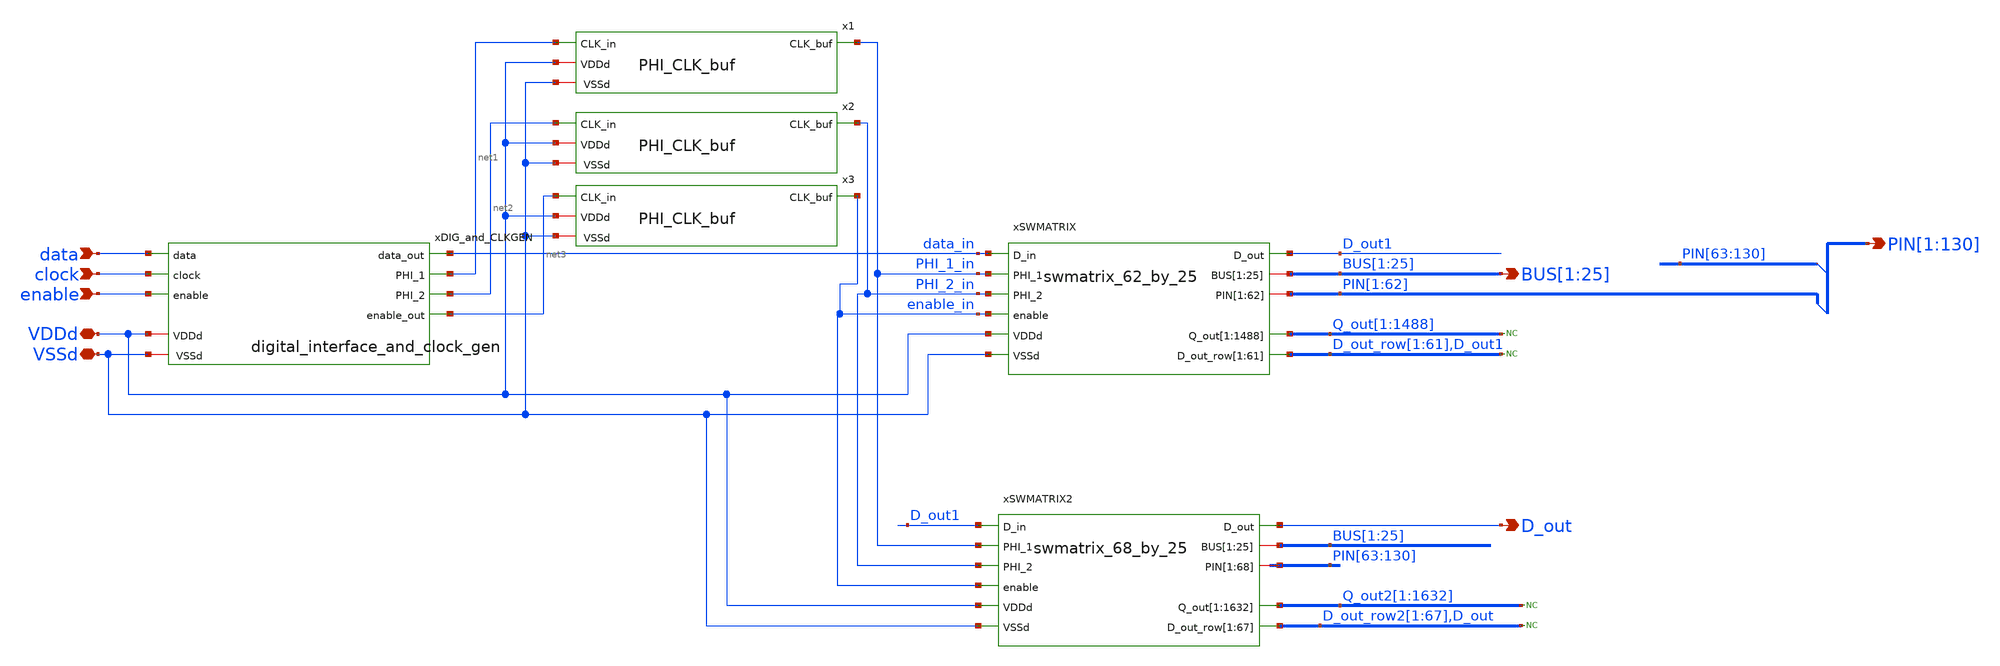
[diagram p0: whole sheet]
** sch_path: full_switch_matrix_130_by_25/full_switch_matrix_130_by_25_no_probes.sch
**.subckt full_switch_matrix_130_by_25_no_probes data clock enable D_out
*+ PIN[1],PIN[2],PIN[3],PIN[4],PIN[5],PIN[6],PIN[7],PIN[8],PIN[9],PIN[10],PIN[11],PIN[12],PIN[13],PIN[14],PIN[15],PIN[16],PIN[17],PIN[18],PIN[19],PIN[20],PIN[21],PIN[22],PIN[23],PIN[24],PIN[25],PIN[26],PIN[27],PIN[28],PIN[29],PIN[30],PIN[31],PIN[32],PIN[33],PIN[34],PIN[35],PIN[36],PIN[37],PIN[38],PIN[39],PIN[40],PIN[41],PIN[42],PIN[43],PIN[44],PIN[45],PIN[46],PIN[47],PIN[48],PIN[49],PIN[50],PIN[51],PIN[52],PIN[53],PIN[54],PIN[55],PIN[56],PIN[57],PIN[58],PIN[59],PIN[60],PIN[61],PIN[62],PIN[63],PIN[64],PIN[65],PIN[66],PIN[67],PIN[68],PIN[69],PIN[70],PIN[71],PIN[72],PIN[73],PIN[74],PIN[75],PIN[76],PIN[77],PIN[78],PIN[79],PIN[80],PIN[81],PIN[82],PIN[83],PIN[84],PIN[85],PIN[86],PIN[87],PIN[88],PIN[89],PIN[90],PIN[91],PIN[92],PIN[93],PIN[94],PIN[95],PIN[96],PIN[97],PIN[98],PIN[99],PIN[100],PIN[101],PIN[102],PIN[103],PIN[104],PIN[105],PIN[106],PIN[107],PIN[108],PIN[109],PIN[110],PIN[111],PIN[112],PIN[113],PIN[114],PIN[115],PIN[116],PIN[117],PIN[118],PIN[119],PIN[120],PIN[121],PIN[122],PIN[123],PIN[124],PIN[125],PIN[126],PIN[127],PIN[128],PIN[129],PIN[130]
*+ BUS[1],BUS[2],BUS[3],BUS[4],BUS[5],BUS[6],BUS[7],BUS[8],BUS[9],BUS[10],BUS[11],BUS[12],BUS[13],BUS[14],BUS[15],BUS[16],BUS[17],BUS[18],BUS[19],BUS[20],BUS[21],BUS[22],BUS[23],BUS[24],BUS[25] VSSd VDDd
*.ipin data
*.ipin clock
*.ipin enable
*.opin D_out
*.opin
*+ PIN[1],PIN[2],PIN[3],PIN[4],PIN[5],PIN[6],PIN[7],PIN[8],PIN[9],PIN[10],PIN[11],PIN[12],PIN[13],PIN[14],PIN[15],PIN[16],PIN[17],PIN[18],PIN[19],PIN[20],PIN[21],PIN[22],PIN[23],PIN[24],PIN[25],PIN[26],PIN[27],PIN[28],PIN[29],PIN[30],PIN[31],PIN[32],PIN[33],PIN[34],PIN[35],PIN[36],PIN[37],PIN[38],PIN[39],PIN[40],PIN[41],PIN[42],PIN[43],PIN[44],PIN[45],PIN[46],PIN[47],PIN[48],PIN[49],PIN[50],PIN[51],PIN[52],PIN[53],PIN[54],PIN[55],PIN[56],PIN[57],PIN[58],PIN[59],PIN[60],PIN[61],PIN[62],PIN[63],PIN[64],PIN[65],PIN[66],PIN[67],PIN[68],PIN[69],PIN[70],PIN[71],PIN[72],PIN[73],PIN[74],PIN[75],PIN[76],PIN[77],PIN[78],PIN[79],PIN[80],PIN[81],PIN[82],PIN[83],PIN[84],PIN[85],PIN[86],PIN[87],PIN[88],PIN[89],PIN[90],PIN[91],PIN[92],PIN[93],PIN[94],PIN[95],PIN[96],PIN[97],PIN[98],PIN[99],PIN[100],PIN[101],PIN[102],PIN[103],PIN[104],PIN[105],PIN[106],PIN[107],PIN[108],PIN[109],PIN[110],PIN[111],PIN[112],PIN[113],PIN[114],PIN[115],PIN[116],PIN[117],PIN[118],PIN[119],PIN[120],PIN[121],PIN[122],PIN[123],PIN[124],PIN[125],PIN[126],PIN[127],PIN[128],PIN[129],PIN[130]
*.opin
*+ BUS[1],BUS[2],BUS[3],BUS[4],BUS[5],BUS[6],BUS[7],BUS[8],BUS[9],BUS[10],BUS[11],BUS[12],BUS[13],BUS[14],BUS[15],BUS[16],BUS[17],BUS[18],BUS[19],BUS[20],BUS[21],BUS[22],BUS[23],BUS[24],BUS[25]
*.iopin VSSd
*.iopin VDDd
xSWMATRIX data_in D_out1 PHI_1_in PHI_2_in BUS[1] BUS[2] BUS[3] BUS[4] BUS[5] BUS[6] BUS[7] BUS[8]
+ BUS[9] BUS[10] BUS[11] BUS[12] BUS[13] BUS[14] BUS[15] BUS[16] BUS[17] BUS[18] BUS[19] BUS[20] BUS[21]
+ BUS[22] BUS[23] BUS[24] BUS[25] PIN[1] PIN[2] PIN[3] PIN[4] PIN[5] PIN[6] PIN[7] PIN[8] PIN[9] PIN[10]
+ PIN[11] PIN[12] PIN[13] PIN[14] PIN[15] PIN[16] PIN[17] PIN[18] PIN[19] PIN[20] PIN[21] PIN[22] PIN[23]
+ PIN[24] PIN[25] PIN[26] PIN[27] PIN[28] PIN[29] PIN[30] PIN[31] PIN[32] PIN[33] PIN[34] PIN[35] PIN[36]
+ PIN[37] PIN[38] PIN[39] PIN[40] PIN[41] PIN[42] PIN[43] PIN[44] PIN[45] PIN[46] PIN[47] PIN[48] PIN[49]
+ PIN[50] PIN[51] PIN[52] PIN[53] PIN[54] PIN[55] PIN[56] PIN[57] PIN[58] PIN[59] PIN[60] PIN[61] PIN[62]
+ VDDd VSSd enable_in Q_out[1] Q_out[2] Q_out[3] Q_out[4] Q_out[5] Q_out[6] Q_out[7] Q_out[8] Q_out[9]
+ Q_out[10] Q_out[11] Q_out[12] Q_out[13] Q_out[14] Q_out[15] Q_out[16] Q_out[17] Q_out[18] Q_out[19] Q_out[20]
+ Q_out[21] Q_out[22] Q_out[23] Q_out[24] Q_out[25] Q_out[26] Q_out[27] Q_out[28] Q_out[29] Q_out[30] Q_out[31]
+ Q_out[32] Q_out[33] Q_out[34] Q_out[35] Q_out[36] Q_out[37] Q_out[38] Q_out[39] Q_out[40] Q_out[41] Q_out[42]
+ Q_out[43] Q_out[44] Q_out[45] Q_out[46] Q_out[47] Q_out[48] Q_out[49] Q_out[50] Q_out[51] Q_out[52] Q_out[53]
+ Q_out[54] Q_out[55] Q_out[56] Q_out[57] Q_out[58] Q_out[59] Q_out[60] Q_out[61] Q_out[62] Q_out[63] Q_out[64]
+ Q_out[65] Q_out[66] Q_out[67] Q_out[68] Q_out[69] Q_out[70] Q_out[71] Q_out[72] Q_out[73] Q_out[74] Q_out[75]
+ Q_out[76] Q_out[77] Q_out[78] Q_out[79] Q_out[80] Q_out[81] Q_out[82] Q_out[83] Q_out[84] Q_out[85] Q_out[86]
+ Q_out[87] Q_out[88] Q_out[89] Q_out[90] Q_out[91] Q_out[92] Q_out[93] Q_out[94] Q_out[95] Q_out[96] Q_out[97]
+ Q_out[98] Q_out[99] Q_out[100] Q_out[101] Q_out[102] Q_out[103] Q_out[104] Q_out[105] Q_out[106] Q_out[107]
+ Q_out[108] Q_out[109] Q_out[110] Q_out[111] Q_out[112] Q_out[113] Q_out[114] Q_out[115] Q_out[116] Q_out[117]
+ Q_out[118] Q_out[119] Q_out[120] Q_out[121] Q_out[122] Q_out[123] Q_out[124] Q_out[125] Q_out[126] Q_out[127]
+ Q_out[128] Q_out[129] Q_out[130] Q_out[131] Q_out[132] Q_out[133] Q_out[134] Q_out[135] Q_out[136] Q_out[137]
+ Q_out[138] Q_out[139] Q_out[140] Q_out[141] Q_out[142] Q_out[143] Q_out[144] Q_out[145] Q_out[146] Q_out[147]
+ Q_out[148] Q_out[149] Q_out[150] Q_out[151] Q_out[152] Q_out[153] Q_out[154] Q_out[155] Q_out[156] Q_out[157]
+ Q_out[158] Q_out[159] Q_out[160] Q_out[161] Q_out[162] Q_out[163] Q_out[164] Q_out[165] Q_out[166] Q_out[167]
+ Q_out[168] Q_out[169] Q_out[170] Q_out[171] Q_out[172] Q_out[173] Q_out[174] Q_out[175] Q_out[176] Q_out[177]
+ Q_out[178] Q_out[179] Q_out[180] Q_out[181] Q_out[182] Q_out[183] Q_out[184] Q_out[185] Q_out[186] Q_out[187]
+ Q_out[188] Q_out[189] Q_out[190] Q_out[191] Q_out[192] Q_out[193] Q_out[194] Q_out[195] Q_out[196] Q_out[197]
+ Q_out[198] Q_out[199] Q_out[200] Q_out[201] Q_out[202] Q_out[203] Q_out[204] Q_out[205] Q_out[206] Q_out[207]
+ Q_out[208] Q_out[209] Q_out[210] Q_out[211] Q_out[212] Q_out[213] Q_out[214] Q_out[215] Q_out[216] Q_out[217]
+ Q_out[218] Q_out[219] Q_out[220] Q_out[221] Q_out[222] Q_out[223] Q_out[224] Q_out[225] Q_out[226] Q_out[227]
+ Q_out[228] Q_out[229] Q_out[230] Q_out[231] Q_out[232] Q_out[233] Q_out[234] Q_out[235] Q_out[236] Q_out[237]
+ Q_out[238] Q_out[239] Q_out[240] Q_out[241] Q_out[242] Q_out[243] Q_out[244] Q_out[245] Q_out[246] Q_out[247]
+ Q_out[248] Q_out[249] Q_out[250] Q_out[251] Q_out[252] Q_out[253] Q_out[254] Q_out[255] Q_out[256] Q_out[257]
+ Q_out[258] Q_out[259] Q_out[260] Q_out[261] Q_out[262] Q_out[263] Q_out[264] Q_out[265] Q_out[266] Q_out[267]
+ Q_out[268] Q_out[269] Q_out[270] Q_out[271] Q_out[272] Q_out[273] Q_out[274] Q_out[275] Q_out[276] Q_out[277]
+ Q_out[278] Q_out[279] Q_out[280] Q_out[281] Q_out[282] Q_out[283] Q_out[284] Q_out[285] Q_out[286] Q_out[287]
+ Q_out[288] Q_out[289] Q_out[290] Q_out[291] Q_out[292] Q_out[293] Q_out[294] Q_out[295] Q_out[296] Q_out[297]
+ Q_out[298] Q_out[299] Q_out[300] Q_out[301] Q_out[302] Q_out[303] Q_out[304] Q_out[305] Q_out[306] Q_out[307]
+ Q_out[308] Q_out[309] Q_out[310] Q_out[311] Q_out[312] Q_out[313] Q_out[314] Q_out[315] Q_out[316] Q_out[317]
+ Q_out[318] Q_out[319] Q_out[320] Q_out[321] Q_out[322] Q_out[323] Q_out[324] Q_out[325] Q_out[326] Q_out[327]
+ Q_out[328] Q_out[329] Q_out[330] Q_out[331] Q_out[332] Q_out[333] Q_out[334] Q_out[335] Q_out[336] Q_out[337]
+ Q_out[338] Q_out[339] Q_out[340] Q_out[341] Q_out[342] Q_out[343] Q_out[344] Q_out[345] Q_out[346] Q_out[347]
+ Q_out[348] Q_out[349] Q_out[350] Q_out[351] Q_out[352] Q_out[353] Q_out[354] Q_out[355] Q_out[356] Q_out[357]
+ Q_out[358] Q_out[359] Q_out[360] Q_out[361] Q_out[362] Q_out[363] Q_out[364] Q_out[365] Q_out[366] Q_out[367]
+ Q_out[368] Q_out[369] Q_out[370] Q_out[371] Q_out[372] Q_out[373] Q_out[374] Q_out[375] Q_out[376] Q_out[377]
+ Q_out[378] Q_out[379] Q_out[380] Q_out[381] Q_out[382] Q_out[383] Q_out[384] Q_out[385] Q_out[386] Q_out[387]
+ Q_out[388] Q_out[389] Q_out[390] Q_out[391] Q_out[392] Q_out[393] Q_out[394] Q_out[395] Q_out[396] Q_out[397]
+ Q_out[398] Q_out[399] Q_out[400] Q_out[401] Q_out[402] Q_out[403] Q_out[404] Q_out[405] Q_out[406] Q_out[407]
+ Q_out[408] Q_out[409] Q_out[410] Q_out[411] Q_out[412] Q_out[413] Q_out[414] Q_out[415] Q_out[416] Q_out[417]
+ Q_out[418] Q_out[419] Q_out[420] Q_out[421] Q_out[422] Q_out[423] Q_out[424] Q_out[425] Q_out[426] Q_out[427]
+ Q_out[428] Q_out[429] Q_out[430] Q_out[431] Q_out[432] Q_out[433] Q_out[434] Q_out[435] Q_out[436] Q_out[437]
+ Q_out[438] Q_out[439] Q_out[440] Q_out[441] Q_out[442] Q_out[443] Q_out[444] Q_out[445] Q_out[446] Q_out[447]
+ Q_out[448] Q_out[449] Q_out[450] Q_out[451] Q_out[452] Q_out[453] Q_out[454] Q_out[455] Q_out[456] Q_out[457]
+ Q_out[458] Q_out[459] Q_out[460] Q_out[461] Q_out[462] Q_out[463] Q_out[464] Q_out[465] Q_out[466] Q_out[467]
+ Q_out[468] Q_out[469] Q_out[470] Q_out[471] Q_out[472] Q_out[473] Q_out[474] Q_out[475] Q_out[476] Q_out[477]
+ Q_out[478] Q_out[479] Q_out[480] Q_out[481] Q_out[482] Q_out[483] Q_out[484] Q_out[485] Q_out[486] Q_out[487]
+ Q_out[488] Q_out[489] Q_out[490] Q_out[491] Q_out[492] Q_out[493] Q_out[494] Q_out[495] Q_out[496] Q_out[497]
+ Q_out[498] Q_out[499] Q_out[500] Q_out[501] Q_out[502] Q_out[503] Q_out[504] Q_out[505] Q_out[506] Q_out[507]
+ Q_out[508] Q_out[509] Q_out[510] Q_out[511] Q_out[512] Q_out[513] Q_out[514] Q_out[515] Q_out[516] Q_out[517]
+ Q_out[518] Q_out[519] Q_out[520] Q_out[521] Q_out[522] Q_out[523] Q_out[524] Q_out[525] Q_out[526] Q_out[527]
+ Q_out[528] Q_out[529] Q_out[530] Q_out[531] Q_out[532] Q_out[533] Q_out[534] Q_out[535] Q_out[536] Q_out[537]
+ Q_out[538] Q_out[539] Q_out[540] Q_out[541] Q_out[542] Q_out[543] Q_out[544] Q_out[545] Q_out[546] Q_out[547]
+ Q_out[548] Q_out[549] Q_out[550] Q_out[551] Q_out[552] Q_out[553] Q_out[554] Q_out[555] Q_out[556] Q_out[557]
+ Q_out[558] Q_out[559] Q_out[560] Q_out[561] Q_out[562] Q_out[563] Q_out[564] Q_out[565] Q_out[566] Q_out[567]
+ Q_out[568] Q_out[569] Q_out[570] Q_out[571] Q_out[572] Q_out[573] Q_out[574] Q_out[575] Q_out[576] Q_out[577]
+ Q_out[578] Q_out[579] Q_out[580] Q_out[581] Q_out[582] Q_out[583] Q_out[584] Q_out[585] Q_out[586] Q_out[587]
+ Q_out[588] Q_out[589] Q_out[590] Q_out[591] Q_out[592] Q_out[593] Q_out[594] Q_out[595] Q_out[596] Q_out[597]
+ Q_out[598] Q_out[599] Q_out[600] Q_out[601] Q_out[602] Q_out[603] Q_out[604] Q_out[605] Q_out[606] Q_out[607]
+ Q_out[608] Q_out[609] Q_out[610] Q_out[611] Q_out[612] Q_out[613] Q_out[614] Q_out[615] Q_out[616] Q_out[617]
+ Q_out[618] Q_out[619] Q_out[620] Q_out[621] Q_out[622] Q_out[623] Q_out[624] Q_out[625] Q_out[626] Q_out[627]
+ Q_out[628] Q_out[629] Q_out[630] Q_out[631] Q_out[632] Q_out[633] Q_out[634] Q_out[635] Q_out[636] Q_out[637]
+ Q_out[638] Q_out[639] Q_out[640] Q_out[641] Q_out[642] Q_out[643] Q_out[644] Q_out[645] Q_out[646] Q_out[647]
+ Q_out[648] Q_out[649] Q_out[650] Q_out[651] Q_out[652] Q_out[653] Q_out[654] Q_out[655] Q_out[656] Q_out[657]
+ Q_out[658] Q_out[659] Q_out[660] Q_out[661] Q_out[662] Q_out[663] Q_out[664] Q_out[665] Q_out[666] Q_out[667]
+ Q_out[668] Q_out[669] Q_out[670] Q_out[671] Q_out[672] Q_out[673] Q_out[674] Q_out[675] Q_out[676] Q_out[677]
+ Q_out[678] Q_out[679] Q_out[680] Q_out[681] Q_out[682] Q_out[683] Q_out[684] Q_out[685] Q_out[686] Q_out[687]
+ Q_out[688] Q_out[689] Q_out[690] Q_out[691] Q_out[692] Q_out[693] Q_out[694] Q_out[695] Q_out[696] Q_out[697]
+ Q_out[698] Q_out[699] Q_out[700] Q_out[701] Q_out[702] Q_out[703] Q_out[704] Q_out[705] Q_out[706] Q_out[707]
+ Q_out[708] Q_out[709] Q_out[710] Q_out[711] Q_out[712] Q_out[713] Q_out[714] Q_out[715] Q_out[716] Q_out[717]
+ Q_out[718] Q_out[719] Q_out[720] Q_out[721] Q_out[722] Q_out[723] Q_out[724] Q_out[725] Q_out[726] Q_out[727]
+ Q_out[728] Q_out[729] Q_out[730] Q_out[731] Q_out[732] Q_out[733] Q_out[734] Q_out[735] Q_out[736] Q_out[737]
+ Q_out[738] Q_out[739] Q_out[740] Q_out[741] Q_out[742] Q_out[743] Q_out[744] Q_out[745] Q_out[746] Q_out[747]
+ Q_out[748] Q_out[749] Q_out[750] Q_out[751] Q_out[752] Q_out[753] Q_out[754] Q_out[755] Q_out[756] Q_out[757]
+ Q_out[758] Q_out[759] Q_out[760] Q_out[761] Q_out[762] Q_out[763] Q_out[764] Q_out[765] Q_out[766] Q_out[767]
+ Q_out[768] Q_out[769] Q_out[770] Q_out[771] Q_out[772] Q_out[773] Q_out[774] Q_out[775] Q_out[776] Q_out[777]
+ Q_out[778] Q_out[779] Q_out[780] Q_out[781] Q_out[782] Q_out[783] Q_out[784] Q_out[785] Q_out[786] Q_out[787]
+ Q_out[788] Q_out[789] Q_out[790] Q_out[791] Q_out[792] Q_out[793] Q_out[794] Q_out[795] Q_out[796] Q_out[797]
+ Q_out[798] Q_out[799] Q_out[800] Q_out[801] Q_out[802] Q_out[803] Q_out[804] Q_out[805] Q_out[806] Q_out[807]
+ Q_out[808] Q_out[809] Q_out[810] Q_out[811] Q_out[812] Q_out[813] Q_out[814] Q_out[815] Q_out[816] Q_out[817]
+ Q_out[818] Q_out[819] Q_out[820] Q_out[821] Q_out[822] Q_out[823] Q_out[824] Q_out[825] Q_out[826] Q_out[827]
+ Q_out[828] Q_out[829] Q_out[830] Q_out[831] Q_out[832] Q_out[833] Q_out[834] Q_out[835] Q_out[836] Q_out[837]
+ Q_out[838] Q_out[839] Q_out[840] Q_out[841] Q_out[842] Q_out[843] Q_out[844] Q_out[845] Q_out[846] Q_out[847]
+ Q_out[848] Q_out[849] Q_out[850] Q_out[851] Q_out[852] Q_out[853] Q_out[854] Q_out[855] Q_out[856] Q_out[857]
+ Q_out[858] Q_out[859] Q_out[860] Q_out[861] Q_out[862] Q_out[863] Q_out[864] Q_out[865] Q_out[866] Q_out[867]
+ Q_out[868] Q_out[869] Q_out[870] Q_out[871] Q_out[872] Q_out[873] Q_out[874] Q_out[875] Q_out[876] Q_out[877]
+ Q_out[878] Q_out[879] Q_out[880] Q_out[881] Q_out[882] Q_out[883] Q_out[884] Q_out[885] Q_out[886] Q_out[887]
+ Q_out[888] Q_out[889] Q_out[890] Q_out[891] Q_out[892] Q_out[893] Q_out[894] Q_out[895] Q_out[896] Q_out[897]
+ Q_out[898] Q_out[899] Q_out[900] Q_out[901] Q_out[902] Q_out[903] Q_out[904] Q_out[905] Q_out[906] Q_out[907]
+ Q_out[908] Q_out[909] Q_out[910] Q_out[911] Q_out[912] Q_out[913] Q_out[914] Q_out[915] Q_out[916] Q_out[917]
+ Q_out[918] Q_out[919] Q_out[920] Q_out[921] Q_out[922] Q_out[923] Q_out[924] Q_out[925] Q_out[926] Q_out[927]
+ Q_out[928] Q_out[929] Q_out[930] Q_out[931] Q_out[932] Q_out[933] Q_out[934] Q_out[935] Q_out[936] Q_out[937]
+ Q_out[938] Q_out[939] Q_out[940] Q_out[941] Q_out[942] Q_out[943] Q_out[944] Q_out[945] Q_out[946] Q_out[947]
+ Q_out[948] Q_out[949] Q_out[950] Q_out[951] Q_out[952] Q_out[953] Q_out[954] Q_out[955] Q_out[956] Q_out[957]
+ Q_out[958] Q_out[959] Q_out[960] Q_out[961] Q_out[962] Q_out[963] Q_out[964] Q_out[965] Q_out[966] Q_out[967]
+ Q_out[968] Q_out[969] Q_out[970] Q_out[971] Q_out[972] Q_out[973] Q_out[974] Q_out[975] Q_out[976] Q_out[977]
+ Q_out[978] Q_out[979] Q_out[980] Q_out[981] Q_out[982] Q_out[983] Q_out[984] Q_out[985] Q_out[986] Q_out[987]
+ Q_out[988] Q_out[989] Q_out[990] Q_out[991] Q_out[992] Q_out[993] Q_out[994] Q_out[995] Q_out[996] Q_out[997]
+ Q_out[998] Q_out[999] Q_out[1000] Q_out[1001] Q_out[1002] Q_out[1003] Q_out[1004] Q_out[1005] Q_out[1006]
+ Q_out[1007] Q_out[1008] Q_out[1009] Q_out[1010] Q_out[1011] Q_out[1012] Q_out[1013] Q_out[1014] Q_out[1015]
+ Q_out[1016] Q_out[1017] Q_out[1018] Q_out[1019] Q_out[1020] Q_out[1021] Q_out[1022] Q_out[1023] Q_out[1024]
+ Q_out[1025] Q_out[1026] Q_out[1027] Q_out[1028] Q_out[1029] Q_out[1030] Q_out[1031] Q_out[1032] Q_out[1033]
+ Q_out[1034] Q_out[1035] Q_out[1036] Q_out[1037] Q_out[1038] Q_out[1039] Q_out[1040] Q_out[1041] Q_out[1042]
+ Q_out[1043] Q_out[1044] Q_out[1045] Q_out[1046] Q_out[1047] Q_out[1048] Q_out[1049] Q_out[1050] Q_out[1051]
+ Q_out[1052] Q_out[1053] Q_out[1054] Q_out[1055] Q_out[1056] Q_out[1057] Q_out[1058] Q_out[1059] Q_out[1060]
+ Q_out[1061] Q_out[1062] Q_out[1063] Q_out[1064] Q_out[1065] Q_out[1066] Q_out[1067] Q_out[1068] Q_out[1069]
+ Q_out[1070] Q_out[1071] Q_out[1072] Q_out[1073] Q_out[1074] Q_out[1075] Q_out[1076] Q_out[1077] Q_out[1078]
+ Q_out[1079] Q_out[1080] Q_out[1081] Q_out[1082] Q_out[1083] Q_out[1084] Q_out[1085] Q_out[1086] Q_out[1087]
+ Q_out[1088] Q_out[1089] Q_out[1090] Q_out[1091] Q_out[1092] Q_out[1093] Q_out[1094] Q_out[1095] Q_out[1096]
+ Q_out[1097] Q_out[1098] Q_out[1099] Q_out[1100] Q_out[1101] Q_out[1102] Q_out[1103] Q_out[1104] Q_out[1105]
+ Q_out[1106] Q_out[1107] Q_out[1108] Q_out[1109] Q_out[1110] Q_out[1111] Q_out[1112] Q_out[1113] Q_out[1114]
+ Q_out[1115] Q_out[1116] Q_out[1117] Q_out[1118] Q_out[1119] Q_out[1120] Q_out[1121] Q_out[1122] Q_out[1123]
+ Q_out[1124] Q_out[1125] Q_out[1126] Q_out[1127] Q_out[1128] Q_out[1129] Q_out[1130] Q_out[1131] Q_out[1132]
+ Q_out[1133] Q_out[1134] Q_out[1135] Q_out[1136] Q_out[1137] Q_out[1138] Q_out[1139] Q_out[1140] Q_out[1141]
+ Q_out[1142] Q_out[1143] Q_out[1144] Q_out[1145] Q_out[1146] Q_out[1147] Q_out[1148] Q_out[1149] Q_out[1150]
+ Q_out[1151] Q_out[1152] Q_out[1153] Q_out[1154] Q_out[1155] Q_out[1156] Q_out[1157] Q_out[1158] Q_out[1159]
+ Q_out[1160] Q_out[1161] Q_out[1162] Q_out[1163] Q_out[1164] Q_out[1165] Q_out[1166] Q_out[1167] Q_out[1168]
+ Q_out[1169] Q_out[1170] Q_out[1171] Q_out[1172] Q_out[1173] Q_out[1174] Q_out[1175] Q_out[1176] Q_out[1177]
+ Q_out[1178] Q_out[1179] Q_out[1180] Q_out[1181] Q_out[1182] Q_out[1183] Q_out[1184] Q_out[1185] Q_out[1186]
+ Q_out[1187] Q_out[1188] Q_out[1189] Q_out[1190] Q_out[1191] Q_out[1192] Q_out[1193] Q_out[1194] Q_out[1195]
+ Q_out[1196] Q_out[1197] Q_out[1198] Q_out[1199] Q_out[1200] Q_out[1201] Q_out[1202] Q_out[1203] Q_out[1204]
+ Q_out[1205] Q_out[1206] Q_out[1207] Q_out[1208] Q_out[1209] Q_out[1210] Q_out[1211] Q_out[1212] Q_out[1213]
+ Q_out[1214] Q_out[1215] Q_out[1216] Q_out[1217] Q_out[1218] Q_out[1219] Q_out[1220] Q_out[1221] Q_out[1222]
+ Q_out[1223] Q_out[1224] Q_out[1225] Q_out[1226] Q_out[1227] Q_out[1228] Q_out[1229] Q_out[1230] Q_out[1231]
+ Q_out[1232] Q_out[1233] Q_out[1234] Q_out[1235] Q_out[1236] Q_out[1237] Q_out[1238] Q_out[1239] Q_out[1240]
+ Q_out[1241] Q_out[1242] Q_out[1243] Q_out[1244] Q_out[1245] Q_out[1246] Q_out[1247] Q_out[1248] Q_out[1249]
+ Q_out[1250] Q_out[1251] Q_out[1252] Q_out[1253] Q_out[1254] Q_out[1255] Q_out[1256] Q_out[1257] Q_out[1258]
+ Q_out[1259] Q_out[1260] Q_out[1261] Q_out[1262] Q_out[1263] Q_out[1264] Q_out[1265] Q_out[1266] Q_out[1267]
+ Q_out[1268] Q_out[1269] Q_out[1270] Q_out[1271] Q_out[1272] Q_out[1273] Q_out[1274] Q_out[1275] Q_out[1276]
+ Q_out[1277] Q_out[1278] Q_out[1279] Q_out[1280] Q_out[1281] Q_out[1282] Q_out[1283] Q_out[1284] Q_out[1285]
+ Q_out[1286] Q_out[1287] Q_out[1288] Q_out[1289] Q_out[1290] Q_out[1291] Q_out[1292] Q_out[1293] Q_out[1294]
+ Q_out[1295] Q_out[1296] Q_out[1297] Q_out[1298] Q_out[1299] Q_out[1300] Q_out[1301] Q_out[1302] Q_out[1303]
+ Q_out[1304] Q_out[1305] Q_out[1306] Q_out[1307] Q_out[1308] Q_out[1309] Q_out[1310] Q_out[1311] Q_out[1312]
+ Q_out[1313] Q_out[1314] Q_out[1315] Q_out[1316] Q_out[1317] Q_out[1318] Q_out[1319] Q_out[1320] Q_out[1321]
+ Q_out[1322] Q_out[1323] Q_out[1324] Q_out[1325] Q_out[1326] Q_out[1327] Q_out[1328] Q_out[1329] Q_out[1330]
+ Q_out[1331] Q_out[1332] Q_out[1333] Q_out[1334] Q_out[1335] Q_out[1336] Q_out[1337] Q_out[1338] Q_out[1339]
+ Q_out[1340] Q_out[1341] Q_out[1342] Q_out[1343] Q_out[1344] Q_out[1345] Q_out[1346] Q_out[1347] Q_out[1348]
+ Q_out[1349] Q_out[1350] Q_out[1351] Q_out[1352] Q_out[1353] Q_out[1354] Q_out[1355] Q_out[1356] Q_out[1357]
+ Q_out[1358] Q_out[1359] Q_out[1360] Q_out[1361] Q_out[1362] Q_out[1363] Q_out[1364] Q_out[1365] Q_out[1366]
+ Q_out[1367] Q_out[1368] Q_out[1369] Q_out[1370] Q_out[1371] Q_out[1372] Q_out[1373] Q_out[1374] Q_out[1375]
+ Q_out[1376] Q_out[1377] Q_out[1378] Q_out[1379] Q_out[1380] Q_out[1381] Q_out[1382] Q_out[1383] Q_out[1384]
+ Q_out[1385] Q_out[1386] Q_out[1387] Q_out[1388] Q_out[1389] Q_out[1390] Q_out[1391] Q_out[1392] Q_out[1393]
+ Q_out[1394] Q_out[1395] Q_out[1396] Q_out[1397] Q_out[1398] Q_out[1399] Q_out[1400] Q_out[1401] Q_out[1402]
+ Q_out[1403] Q_out[1404] Q_out[1405] Q_out[1406] Q_out[1407] Q_out[1408] Q_out[1409] Q_out[1410] Q_out[1411]
+ Q_out[1412] Q_out[1413] Q_out[1414] Q_out[1415] Q_out[1416] Q_out[1417] Q_out[1418] Q_out[1419] Q_out[1420]
+ Q_out[1421] Q_out[1422] Q_out[1423] Q_out[1424] Q_out[1425] Q_out[1426] Q_out[1427] Q_out[1428] Q_out[1429]
+ Q_out[1430] Q_out[1431] Q_out[1432] Q_out[1433] Q_out[1434] Q_out[1435] Q_out[1436] Q_out[1437] Q_out[1438]
+ Q_out[1439] Q_out[1440] Q_out[1441] Q_out[1442] Q_out[1443] Q_out[1444] Q_out[1445] Q_out[1446] Q_out[1447]
+ Q_out[1448] Q_out[1449] Q_out[1450] Q_out[1451] Q_out[1452] Q_out[1453] Q_out[1454] Q_out[1455] Q_out[1456]
+ Q_out[1457] Q_out[1458] Q_out[1459] Q_out[1460] Q_out[1461] Q_out[1462] Q_out[1463] Q_out[1464] Q_out[1465]
+ Q_out[1466] Q_out[1467] Q_out[1468] Q_out[1469] Q_out[1470] Q_out[1471] Q_out[1472] Q_out[1473] Q_out[1474]
+ Q_out[1475] Q_out[1476] Q_out[1477] Q_out[1478] Q_out[1479] Q_out[1480] Q_out[1481] Q_out[1482] Q_out[1483]
+ Q_out[1484] Q_out[1485] Q_out[1486] Q_out[1487] Q_out[1488] D_out_row[1] D_out_row[2] D_out_row[3] D_out_row[4]
+ D_out_row[5] D_out_row[6] D_out_row[7] D_out_row[8] D_out_row[9] D_out_row[10] D_out_row[11] D_out_row[12]
+ D_out_row[13] D_out_row[14] D_out_row[15] D_out_row[16] D_out_row[17] D_out_row[18] D_out_row[19] D_out_row[20]
+ D_out_row[21] D_out_row[22] D_out_row[23] D_out_row[24] D_out_row[25] D_out_row[26] D_out_row[27] D_out_row[28]
+ D_out_row[29] D_out_row[30] D_out_row[31] D_out_row[32] D_out_row[33] D_out_row[34] D_out_row[35] D_out_row[36]
+ D_out_row[37] D_out_row[38] D_out_row[39] D_out_row[40] D_out_row[41] D_out_row[42] D_out_row[43] D_out_row[44]
+ D_out_row[45] D_out_row[46] D_out_row[47] D_out_row[48] D_out_row[49] D_out_row[50] D_out_row[51] D_out_row[52]
+ D_out_row[53] D_out_row[54] D_out_row[55] D_out_row[56] D_out_row[57] D_out_row[58] D_out_row[59] D_out_row[60]
+ D_out_row[61] swmatrix_62_by_25
xDIG_and_CLKGEN data data_in clock net1 net2 enable net3 VDDd VSSd digital_interface_and_clock_gen
x1 PHI_1_in net1 VDDd VSSd PHI_CLK_buf
x2 PHI_2_in net2 VDDd VSSd PHI_CLK_buf
xSWMATRIX2 D_out1 D_out PHI_1_in PHI_2_in BUS[1] BUS[2] BUS[3] BUS[4] BUS[5] BUS[6] BUS[7] BUS[8]
+ BUS[9] BUS[10] BUS[11] BUS[12] BUS[13] BUS[14] BUS[15] BUS[16] BUS[17] BUS[18] BUS[19] BUS[20] BUS[21]
+ BUS[22] BUS[23] BUS[24] BUS[25] PIN[63] PIN[64] PIN[65] PIN[66] PIN[67] PIN[68] PIN[69] PIN[70] PIN[71]
+ PIN[72] PIN[73] PIN[74] PIN[75] PIN[76] PIN[77] PIN[78] PIN[79] PIN[80] PIN[81] PIN[82] PIN[83] PIN[84]
+ PIN[85] PIN[86] PIN[87] PIN[88] PIN[89] PIN[90] PIN[91] PIN[92] PIN[93] PIN[94] PIN[95] PIN[96] PIN[97]
+ PIN[98] PIN[99] PIN[100] PIN[101] PIN[102] PIN[103] PIN[104] PIN[105] PIN[106] PIN[107] PIN[108] PIN[109]
+ PIN[110] PIN[111] PIN[112] PIN[113] PIN[114] PIN[115] PIN[116] PIN[117] PIN[118] PIN[119] PIN[120] PIN[121]
+ PIN[122] PIN[123] PIN[124] PIN[125] PIN[126] PIN[127] PIN[128] PIN[129] PIN[130] VDDd VSSd enable_in
+ Q_out2[1] Q_out2[2] Q_out2[3] Q_out2[4] Q_out2[5] Q_out2[6] Q_out2[7] Q_out2[8] Q_out2[9] Q_out2[10]
+ Q_out2[11] Q_out2[12] Q_out2[13] Q_out2[14] Q_out2[15] Q_out2[16] Q_out2[17] Q_out2[18] Q_out2[19] Q_out2[20]
+ Q_out2[21] Q_out2[22] Q_out2[23] Q_out2[24] Q_out2[25] Q_out2[26] Q_out2[27] Q_out2[28] Q_out2[29] Q_out2[30]
+ Q_out2[31] Q_out2[32] Q_out2[33] Q_out2[34] Q_out2[35] Q_out2[36] Q_out2[37] Q_out2[38] Q_out2[39] Q_out2[40]
+ Q_out2[41] Q_out2[42] Q_out2[43] Q_out2[44] Q_out2[45] Q_out2[46] Q_out2[47] Q_out2[48] Q_out2[49] Q_out2[50]
+ Q_out2[51] Q_out2[52] Q_out2[53] Q_out2[54] Q_out2[55] Q_out2[56] Q_out2[57] Q_out2[58] Q_out2[59] Q_out2[60]
+ Q_out2[61] Q_out2[62] Q_out2[63] Q_out2[64] Q_out2[65] Q_out2[66] Q_out2[67] Q_out2[68] Q_out2[69] Q_out2[70]
+ Q_out2[71] Q_out2[72] Q_out2[73] Q_out2[74] Q_out2[75] Q_out2[76] Q_out2[77] Q_out2[78] Q_out2[79] Q_out2[80]
+ Q_out2[81] Q_out2[82] Q_out2[83] Q_out2[84] Q_out2[85] Q_out2[86] Q_out2[87] Q_out2[88] Q_out2[89] Q_out2[90]
+ Q_out2[91] Q_out2[92] Q_out2[93] Q_out2[94] Q_out2[95] Q_out2[96] Q_out2[97] Q_out2[98] Q_out2[99] Q_out2[100]
+ Q_out2[101] Q_out2[102] Q_out2[103] Q_out2[104] Q_out2[105] Q_out2[106] Q_out2[107] Q_out2[108] Q_out2[109]
+ Q_out2[110] Q_out2[111] Q_out2[112] Q_out2[113] Q_out2[114] Q_out2[115] Q_out2[116] Q_out2[117] Q_out2[118]
+ Q_out2[119] Q_out2[120] Q_out2[121] Q_out2[122] Q_out2[123] Q_out2[124] Q_out2[125] Q_out2[126] Q_out2[127]
+ Q_out2[128] Q_out2[129] Q_out2[130] Q_out2[131] Q_out2[132] Q_out2[133] Q_out2[134] Q_out2[135] Q_out2[136]
+ Q_out2[137] Q_out2[138] Q_out2[139] Q_out2[140] Q_out2[141] Q_out2[142] Q_out2[143] Q_out2[144] Q_out2[145]
+ Q_out2[146] Q_out2[147] Q_out2[148] Q_out2[149] Q_out2[150] Q_out2[151] Q_out2[152] Q_out2[153] Q_out2[154]
+ Q_out2[155] Q_out2[156] Q_out2[157] Q_out2[158] Q_out2[159] Q_out2[160] Q_out2[161] Q_out2[162] Q_out2[163]
+ Q_out2[164] Q_out2[165] Q_out2[166] Q_out2[167] Q_out2[168] Q_out2[169] Q_out2[170] Q_out2[171] Q_out2[172]
+ Q_out2[173] Q_out2[174] Q_out2[175] Q_out2[176] Q_out2[177] Q_out2[178] Q_out2[179] Q_out2[180] Q_out2[181]
+ Q_out2[182] Q_out2[183] Q_out2[184] Q_out2[185] Q_out2[186] Q_out2[187] Q_out2[188] Q_out2[189] Q_out2[190]
+ Q_out2[191] Q_out2[192] Q_out2[193] Q_out2[194] Q_out2[195] Q_out2[196] Q_out2[197] Q_out2[198] Q_out2[199]
+ Q_out2[200] Q_out2[201] Q_out2[202] Q_out2[203] Q_out2[204] Q_out2[205] Q_out2[206] Q_out2[207] Q_out2[208]
+ Q_out2[209] Q_out2[210] Q_out2[211] Q_out2[212] Q_out2[213] Q_out2[214] Q_out2[215] Q_out2[216] Q_out2[217]
+ Q_out2[218] Q_out2[219] Q_out2[220] Q_out2[221] Q_out2[222] Q_out2[223] Q_out2[224] Q_out2[225] Q_out2[226]
+ Q_out2[227] Q_out2[228] Q_out2[229] Q_out2[230] Q_out2[231] Q_out2[232] Q_out2[233] Q_out2[234] Q_out2[235]
+ Q_out2[236] Q_out2[237] Q_out2[238] Q_out2[239] Q_out2[240] Q_out2[241] Q_out2[242] Q_out2[243] Q_out2[244]
+ Q_out2[245] Q_out2[246] Q_out2[247] Q_out2[248] Q_out2[249] Q_out2[250] Q_out2[251] Q_out2[252] Q_out2[253]
+ Q_out2[254] Q_out2[255] Q_out2[256] Q_out2[257] Q_out2[258] Q_out2[259] Q_out2[260] Q_out2[261] Q_out2[262]
+ Q_out2[263] Q_out2[264] Q_out2[265] Q_out2[266] Q_out2[267] Q_out2[268] Q_out2[269] Q_out2[270] Q_out2[271]
+ Q_out2[272] Q_out2[273] Q_out2[274] Q_out2[275] Q_out2[276] Q_out2[277] Q_out2[278] Q_out2[279] Q_out2[280]
+ Q_out2[281] Q_out2[282] Q_out2[283] Q_out2[284] Q_out2[285] Q_out2[286] Q_out2[287] Q_out2[288] Q_out2[289]
+ Q_out2[290] Q_out2[291] Q_out2[292] Q_out2[293] Q_out2[294] Q_out2[295] Q_out2[296] Q_out2[297] Q_out2[298]
+ Q_out2[299] Q_out2[300] Q_out2[301] Q_out2[302] Q_out2[303] Q_out2[304] Q_out2[305] Q_out2[306] Q_out2[307]
+ Q_out2[308] Q_out2[309] Q_out2[310] Q_out2[311] Q_out2[312] Q_out2[313] Q_out2[314] Q_out2[315] Q_out2[316]
+ Q_out2[317] Q_out2[318] Q_out2[319] Q_out2[320] Q_out2[321] Q_out2[322] Q_out2[323] Q_out2[324] Q_out2[325]
+ Q_out2[326] Q_out2[327] Q_out2[328] Q_out2[329] Q_out2[330] Q_out2[331] Q_out2[332] Q_out2[333] Q_out2[334]
+ Q_out2[335] Q_out2[336] Q_out2[337] Q_out2[338] Q_out2[339] Q_out2[340] Q_out2[341] Q_out2[342] Q_out2[343]
+ Q_out2[344] Q_out2[345] Q_out2[346] Q_out2[347] Q_out2[348] Q_out2[349] Q_out2[350] Q_out2[351] Q_out2[352]
+ Q_out2[353] Q_out2[354] Q_out2[355] Q_out2[356] Q_out2[357] Q_out2[358] Q_out2[359] Q_out2[360] Q_out2[361]
+ Q_out2[362] Q_out2[363] Q_out2[364] Q_out2[365] Q_out2[366] Q_out2[367] Q_out2[368] Q_out2[369] Q_out2[370]
+ Q_out2[371] Q_out2[372] Q_out2[373] Q_out2[374] Q_out2[375] Q_out2[376] Q_out2[377] Q_out2[378] Q_out2[379]
+ Q_out2[380] Q_out2[381] Q_out2[382] Q_out2[383] Q_out2[384] Q_out2[385] Q_out2[386] Q_out2[387] Q_out2[388]
+ Q_out2[389] Q_out2[390] Q_out2[391] Q_out2[392] Q_out2[393] Q_out2[394] Q_out2[395] Q_out2[396] Q_out2[397]
+ Q_out2[398] Q_out2[399] Q_out2[400] Q_out2[401] Q_out2[402] Q_out2[403] Q_out2[404] Q_out2[405] Q_out2[406]
+ Q_out2[407] Q_out2[408] Q_out2[409] Q_out2[410] Q_out2[411] Q_out2[412] Q_out2[413] Q_out2[414] Q_out2[415]
+ Q_out2[416] Q_out2[417] Q_out2[418] Q_out2[419] Q_out2[420] Q_out2[421] Q_out2[422] Q_out2[423] Q_out2[424]
+ Q_out2[425] Q_out2[426] Q_out2[427] Q_out2[428] Q_out2[429] Q_out2[430] Q_out2[431] Q_out2[432] Q_out2[433]
+ Q_out2[434] Q_out2[435] Q_out2[436] Q_out2[437] Q_out2[438] Q_out2[439] Q_out2[440] Q_out2[441] Q_out2[442]
+ Q_out2[443] Q_out2[444] Q_out2[445] Q_out2[446] Q_out2[447] Q_out2[448] Q_out2[449] Q_out2[450] Q_out2[451]
+ Q_out2[452] Q_out2[453] Q_out2[454] Q_out2[455] Q_out2[456] Q_out2[457] Q_out2[458] Q_out2[459] Q_out2[460]
+ Q_out2[461] Q_out2[462] Q_out2[463] Q_out2[464] Q_out2[465] Q_out2[466] Q_out2[467] Q_out2[468] Q_out2[469]
+ Q_out2[470] Q_out2[471] Q_out2[472] Q_out2[473] Q_out2[474] Q_out2[475] Q_out2[476] Q_out2[477] Q_out2[478]
+ Q_out2[479] Q_out2[480] Q_out2[481] Q_out2[482] Q_out2[483] Q_out2[484] Q_out2[485] Q_out2[486] Q_out2[487]
+ Q_out2[488] Q_out2[489] Q_out2[490] Q_out2[491] Q_out2[492] Q_out2[493] Q_out2[494] Q_out2[495] Q_out2[496]
+ Q_out2[497] Q_out2[498] Q_out2[499] Q_out2[500] Q_out2[501] Q_out2[502] Q_out2[503] Q_out2[504] Q_out2[505]
+ Q_out2[506] Q_out2[507] Q_out2[508] Q_out2[509] Q_out2[510] Q_out2[511] Q_out2[512] Q_out2[513] Q_out2[514]
+ Q_out2[515] Q_out2[516] Q_out2[517] Q_out2[518] Q_out2[519] Q_out2[520] Q_out2[521] Q_out2[522] Q_out2[523]
+ Q_out2[524] Q_out2[525] Q_out2[526] Q_out2[527] Q_out2[528] Q_out2[529] Q_out2[530] Q_out2[531] Q_out2[532]
+ Q_out2[533] Q_out2[534] Q_out2[535] Q_out2[536] Q_out2[537] Q_out2[538] Q_out2[539] Q_out2[540] Q_out2[541]
+ Q_out2[542] Q_out2[543] Q_out2[544] Q_out2[545] Q_out2[546] Q_out2[547] Q_out2[548] Q_out2[549] Q_out2[550]
+ Q_out2[551] Q_out2[552] Q_out2[553] Q_out2[554] Q_out2[555] Q_out2[556] Q_out2[557] Q_out2[558] Q_out2[559]
+ Q_out2[560] Q_out2[561] Q_out2[562] Q_out2[563] Q_out2[564] Q_out2[565] Q_out2[566] Q_out2[567] Q_out2[568]
+ Q_out2[569] Q_out2[570] Q_out2[571] Q_out2[572] Q_out2[573] Q_out2[574] Q_out2[575] Q_out2[576] Q_out2[577]
+ Q_out2[578] Q_out2[579] Q_out2[580] Q_out2[581] Q_out2[582] Q_out2[583] Q_out2[584] Q_out2[585] Q_out2[586]
+ Q_out2[587] Q_out2[588] Q_out2[589] Q_out2[590] Q_out2[591] Q_out2[592] Q_out2[593] Q_out2[594] Q_out2[595]
+ Q_out2[596] Q_out2[597] Q_out2[598] Q_out2[599] Q_out2[600] Q_out2[601] Q_out2[602] Q_out2[603] Q_out2[604]
+ Q_out2[605] Q_out2[606] Q_out2[607] Q_out2[608] Q_out2[609] Q_out2[610] Q_out2[611] Q_out2[612] Q_out2[613]
+ Q_out2[614] Q_out2[615] Q_out2[616] Q_out2[617] Q_out2[618] Q_out2[619] Q_out2[620] Q_out2[621] Q_out2[622]
+ Q_out2[623] Q_out2[624] Q_out2[625] Q_out2[626] Q_out2[627] Q_out2[628] Q_out2[629] Q_out2[630] Q_out2[631]
+ Q_out2[632] Q_out2[633] Q_out2[634] Q_out2[635] Q_out2[636] Q_out2[637] Q_out2[638] Q_out2[639] Q_out2[640]
+ Q_out2[641] Q_out2[642] Q_out2[643] Q_out2[644] Q_out2[645] Q_out2[646] Q_out2[647] Q_out2[648] Q_out2[649]
+ Q_out2[650] Q_out2[651] Q_out2[652] Q_out2[653] Q_out2[654] Q_out2[655] Q_out2[656] Q_out2[657] Q_out2[658]
+ Q_out2[659] Q_out2[660] Q_out2[661] Q_out2[662] Q_out2[663] Q_out2[664] Q_out2[665] Q_out2[666] Q_out2[667]
+ Q_out2[668] Q_out2[669] Q_out2[670] Q_out2[671] Q_out2[672] Q_out2[673] Q_out2[674] Q_out2[675] Q_out2[676]
+ Q_out2[677] Q_out2[678] Q_out2[679] Q_out2[680] Q_out2[681] Q_out2[682] Q_out2[683] Q_out2[684] Q_out2[685]
+ Q_out2[686] Q_out2[687] Q_out2[688] Q_out2[689] Q_out2[690] Q_out2[691] Q_out2[692] Q_out2[693] Q_out2[694]
+ Q_out2[695] Q_out2[696] Q_out2[697] Q_out2[698] Q_out2[699] Q_out2[700] Q_out2[701] Q_out2[702] Q_out2[703]
+ Q_out2[704] Q_out2[705] Q_out2[706] Q_out2[707] Q_out2[708] Q_out2[709] Q_out2[710] Q_out2[711] Q_out2[712]
+ Q_out2[713] Q_out2[714] Q_out2[715] Q_out2[716] Q_out2[717] Q_out2[718] Q_out2[719] Q_out2[720] Q_out2[721]
+ Q_out2[722] Q_out2[723] Q_out2[724] Q_out2[725] Q_out2[726] Q_out2[727] Q_out2[728] Q_out2[729] Q_out2[730]
+ Q_out2[731] Q_out2[732] Q_out2[733] Q_out2[734] Q_out2[735] Q_out2[736] Q_out2[737] Q_out2[738] Q_out2[739]
+ Q_out2[740] Q_out2[741] Q_out2[742] Q_out2[743] Q_out2[744] Q_out2[745] Q_out2[746] Q_out2[747] Q_out2[748]
+ Q_out2[749] Q_out2[750] Q_out2[751] Q_out2[752] Q_out2[753] Q_out2[754] Q_out2[755] Q_out2[756] Q_out2[757]
+ Q_out2[758] Q_out2[759] Q_out2[760] Q_out2[761] Q_out2[762] Q_out2[763] Q_out2[764] Q_out2[765] Q_out2[766]
+ Q_out2[767] Q_out2[768] Q_out2[769] Q_out2[770] Q_out2[771] Q_out2[772] Q_out2[773] Q_out2[774] Q_out2[775]
+ Q_out2[776] Q_out2[777] Q_out2[778] Q_out2[779] Q_out2[780] Q_out2[781] Q_out2[782] Q_out2[783] Q_out2[784]
+ Q_out2[785] Q_out2[786] Q_out2[787] Q_out2[788] Q_out2[789] Q_out2[790] Q_out2[791] Q_out2[792] Q_out2[793]
+ Q_out2[794] Q_out2[795] Q_out2[796] Q_out2[797] Q_out2[798] Q_out2[799] Q_out2[800] Q_out2[801] Q_out2[802]
+ Q_out2[803] Q_out2[804] Q_out2[805] Q_out2[806] Q_out2[807] Q_out2[808] Q_out2[809] Q_out2[810] Q_out2[811]
+ Q_out2[812] Q_out2[813] Q_out2[814] Q_out2[815] Q_out2[816] Q_out2[817] Q_out2[818] Q_out2[819] Q_out2[820]
+ Q_out2[821] Q_out2[822] Q_out2[823] Q_out2[824] Q_out2[825] Q_out2[826] Q_out2[827] Q_out2[828] Q_out2[829]
+ Q_out2[830] Q_out2[831] Q_out2[832] Q_out2[833] Q_out2[834] Q_out2[835] Q_out2[836] Q_out2[837] Q_out2[838]
+ Q_out2[839] Q_out2[840] Q_out2[841] Q_out2[842] Q_out2[843] Q_out2[844] Q_out2[845] Q_out2[846] Q_out2[847]
+ Q_out2[848] Q_out2[849] Q_out2[850] Q_out2[851] Q_out2[852] Q_out2[853] Q_out2[854] Q_out2[855] Q_out2[856]
+ Q_out2[857] Q_out2[858] Q_out2[859] Q_out2[860] Q_out2[861] Q_out2[862] Q_out2[863] Q_out2[864] Q_out2[865]
+ Q_out2[866] Q_out2[867] Q_out2[868] Q_out2[869] Q_out2[870] Q_out2[871] Q_out2[872] Q_out2[873] Q_out2[874]
+ Q_out2[875] Q_out2[876] Q_out2[877] Q_out2[878] Q_out2[879] Q_out2[880] Q_out2[881] Q_out2[882] Q_out2[883]
+ Q_out2[884] Q_out2[885] Q_out2[886] Q_out2[887] Q_out2[888] Q_out2[889] Q_out2[890] Q_out2[891] Q_out2[892]
+ Q_out2[893] Q_out2[894] Q_out2[895] Q_out2[896] Q_out2[897] Q_out2[898] Q_out2[899] Q_out2[900] Q_out2[901]
+ Q_out2[902] Q_out2[903] Q_out2[904] Q_out2[905] Q_out2[906] Q_out2[907] Q_out2[908] Q_out2[909] Q_out2[910]
+ Q_out2[911] Q_out2[912] Q_out2[913] Q_out2[914] Q_out2[915] Q_out2[916] Q_out2[917] Q_out2[918] Q_out2[919]
+ Q_out2[920] Q_out2[921] Q_out2[922] Q_out2[923] Q_out2[924] Q_out2[925] Q_out2[926] Q_out2[927] Q_out2[928]
+ Q_out2[929] Q_out2[930] Q_out2[931] Q_out2[932] Q_out2[933] Q_out2[934] Q_out2[935] Q_out2[936] Q_out2[937]
+ Q_out2[938] Q_out2[939] Q_out2[940] Q_out2[941] Q_out2[942] Q_out2[943] Q_out2[944] Q_out2[945] Q_out2[946]
+ Q_out2[947] Q_out2[948] Q_out2[949] Q_out2[950] Q_out2[951] Q_out2[952] Q_out2[953] Q_out2[954] Q_out2[955]
+ Q_out2[956] Q_out2[957] Q_out2[958] Q_out2[959] Q_out2[960] Q_out2[961] Q_out2[962] Q_out2[963] Q_out2[964]
+ Q_out2[965] Q_out2[966] Q_out2[967] Q_out2[968] Q_out2[969] Q_out2[970] Q_out2[971] Q_out2[972] Q_out2[973]
+ Q_out2[974] Q_out2[975] Q_out2[976] Q_out2[977] Q_out2[978] Q_out2[979] Q_out2[980] Q_out2[981] Q_out2[982]
+ Q_out2[983] Q_out2[984] Q_out2[985] Q_out2[986] Q_out2[987] Q_out2[988] Q_out2[989] Q_out2[990] Q_out2[991]
+ Q_out2[992] Q_out2[993] Q_out2[994] Q_out2[995] Q_out2[996] Q_out2[997] Q_out2[998] Q_out2[999] Q_out2[1000]
+ Q_out2[1001] Q_out2[1002] Q_out2[1003] Q_out2[1004] Q_out2[1005] Q_out2[1006] Q_out2[1007] Q_out2[1008]
+ Q_out2[1009] Q_out2[1010] Q_out2[1011] Q_out2[1012] Q_out2[1013] Q_out2[1014] Q_out2[1015] Q_out2[1016]
+ Q_out2[1017] Q_out2[1018] Q_out2[1019] Q_out2[1020] Q_out2[1021] Q_out2[1022] Q_out2[1023] Q_out2[1024]
+ Q_out2[1025] Q_out2[1026] Q_out2[1027] Q_out2[1028] Q_out2[1029] Q_out2[1030] Q_out2[1031] Q_out2[1032]
+ Q_out2[1033] Q_out2[1034] Q_out2[1035] Q_out2[1036] Q_out2[1037] Q_out2[1038] Q_out2[1039] Q_out2[1040]
+ Q_out2[1041] Q_out2[1042] Q_out2[1043] Q_out2[1044] Q_out2[1045] Q_out2[1046] Q_out2[1047] Q_out2[1048]
+ Q_out2[1049] Q_out2[1050] Q_out2[1051] Q_out2[1052] Q_out2[1053] Q_out2[1054] Q_out2[1055] Q_out2[1056]
+ Q_out2[1057] Q_out2[1058] Q_out2[1059] Q_out2[1060] Q_out2[1061] Q_out2[1062] Q_out2[1063] Q_out2[1064]
+ Q_out2[1065] Q_out2[1066] Q_out2[1067] Q_out2[1068] Q_out2[1069] Q_out2[1070] Q_out2[1071] Q_out2[1072]
+ Q_out2[1073] Q_out2[1074] Q_out2[1075] Q_out2[1076] Q_out2[1077] Q_out2[1078] Q_out2[1079] Q_out2[1080]
+ Q_out2[1081] Q_out2[1082] Q_out2[1083] Q_out2[1084] Q_out2[1085] Q_out2[1086] Q_out2[1087] Q_out2[1088]
+ Q_out2[1089] Q_out2[1090] Q_out2[1091] Q_out2[1092] Q_out2[1093] Q_out2[1094] Q_out2[1095] Q_out2[1096]
+ Q_out2[1097] Q_out2[1098] Q_out2[1099] Q_out2[1100] Q_out2[1101] Q_out2[1102] Q_out2[1103] Q_out2[1104]
+ Q_out2[1105] Q_out2[1106] Q_out2[1107] Q_out2[1108] Q_out2[1109] Q_out2[1110] Q_out2[1111] Q_out2[1112]
+ Q_out2[1113] Q_out2[1114] Q_out2[1115] Q_out2[1116] Q_out2[1117] Q_out2[1118] Q_out2[1119] Q_out2[1120]
+ Q_out2[1121] Q_out2[1122] Q_out2[1123] Q_out2[1124] Q_out2[1125] Q_out2[1126] Q_out2[1127] Q_out2[1128]
+ Q_out2[1129] Q_out2[1130] Q_out2[1131] Q_out2[1132] Q_out2[1133] Q_out2[1134] Q_out2[1135] Q_out2[1136]
+ Q_out2[1137] Q_out2[1138] Q_out2[1139] Q_out2[1140] Q_out2[1141] Q_out2[1142] Q_out2[1143] Q_out2[1144]
+ Q_out2[1145] Q_out2[1146] Q_out2[1147] Q_out2[1148] Q_out2[1149] Q_out2[1150] Q_out2[1151] Q_out2[1152]
+ Q_out2[1153] Q_out2[1154] Q_out2[1155] Q_out2[1156] Q_out2[1157] Q_out2[1158] Q_out2[1159] Q_out2[1160]
+ Q_out2[1161] Q_out2[1162] Q_out2[1163] Q_out2[1164] Q_out2[1165] Q_out2[1166] Q_out2[1167] Q_out2[1168]
+ Q_out2[1169] Q_out2[1170] Q_out2[1171] Q_out2[1172] Q_out2[1173] Q_out2[1174] Q_out2[1175] Q_out2[1176]
+ Q_out2[1177] Q_out2[1178] Q_out2[1179] Q_out2[1180] Q_out2[1181] Q_out2[1182] Q_out2[1183] Q_out2[1184]
+ Q_out2[1185] Q_out2[1186] Q_out2[1187] Q_out2[1188] Q_out2[1189] Q_out2[1190] Q_out2[1191] Q_out2[1192]
+ Q_out2[1193] Q_out2[1194] Q_out2[1195] Q_out2[1196] Q_out2[1197] Q_out2[1198] Q_out2[1199] Q_out2[1200]
+ Q_out2[1201] Q_out2[1202] Q_out2[1203] Q_out2[1204] Q_out2[1205] Q_out2[1206] Q_out2[1207] Q_out2[1208]
+ Q_out2[1209] Q_out2[1210] Q_out2[1211] Q_out2[1212] Q_out2[1213] Q_out2[1214] Q_out2[1215] Q_out2[1216]
+ Q_out2[1217] Q_out2[1218] Q_out2[1219] Q_out2[1220] Q_out2[1221] Q_out2[1222] Q_out2[1223] Q_out2[1224]
+ Q_out2[1225] Q_out2[1226] Q_out2[1227] Q_out2[1228] Q_out2[1229] Q_out2[1230] Q_out2[1231] Q_out2[1232]
+ Q_out2[1233] Q_out2[1234] Q_out2[1235] Q_out2[1236] Q_out2[1237] Q_out2[1238] Q_out2[1239] Q_out2[1240]
+ Q_out2[1241] Q_out2[1242] Q_out2[1243] Q_out2[1244] Q_out2[1245] Q_out2[1246] Q_out2[1247] Q_out2[1248]
+ Q_out2[1249] Q_out2[1250] Q_out2[1251] Q_out2[1252] Q_out2[1253] Q_out2[1254] Q_out2[1255] Q_out2[1256]
+ Q_out2[1257] Q_out2[1258] Q_out2[1259] Q_out2[1260] Q_out2[1261] Q_out2[1262] Q_out2[1263] Q_out2[1264]
+ Q_out2[1265] Q_out2[1266] Q_out2[1267] Q_out2[1268] Q_out2[1269] Q_out2[1270] Q_out2[1271] Q_out2[1272]
+ Q_out2[1273] Q_out2[1274] Q_out2[1275] Q_out2[1276] Q_out2[1277] Q_out2[1278] Q_out2[1279] Q_out2[1280]
+ Q_out2[1281] Q_out2[1282] Q_out2[1283] Q_out2[1284] Q_out2[1285] Q_out2[1286] Q_out2[1287] Q_out2[1288]
+ Q_out2[1289] Q_out2[1290] Q_out2[1291] Q_out2[1292] Q_out2[1293] Q_out2[1294] Q_out2[1295] Q_out2[1296]
+ Q_out2[1297] Q_out2[1298] Q_out2[1299] Q_out2[1300] Q_out2[1301] Q_out2[1302] Q_out2[1303] Q_out2[1304]
+ Q_out2[1305] Q_out2[1306] Q_out2[1307] Q_out2[1308] Q_out2[1309] Q_out2[1310] Q_out2[1311] Q_out2[1312]
+ Q_out2[1313] Q_out2[1314] Q_out2[1315] Q_out2[1316] Q_out2[1317] Q_out2[1318] Q_out2[1319] Q_out2[1320]
+ Q_out2[1321] Q_out2[1322] Q_out2[1323] Q_out2[1324] Q_out2[1325] Q_out2[1326] Q_out2[1327] Q_out2[1328]
+ Q_out2[1329] Q_out2[1330] Q_out2[1331] Q_out2[1332] Q_out2[1333] Q_out2[1334] Q_out2[1335] Q_out2[1336]
+ Q_out2[1337] Q_out2[1338] Q_out2[1339] Q_out2[1340] Q_out2[1341] Q_out2[1342] Q_out2[1343] Q_out2[1344]
+ Q_out2[1345] Q_out2[1346] Q_out2[1347] Q_out2[1348] Q_out2[1349] Q_out2[1350] Q_out2[1351] Q_out2[1352]
+ Q_out2[1353] Q_out2[1354] Q_out2[1355] Q_out2[1356] Q_out2[1357] Q_out2[1358] Q_out2[1359] Q_out2[1360]
+ Q_out2[1361] Q_out2[1362] Q_out2[1363] Q_out2[1364] Q_out2[1365] Q_out2[1366] Q_out2[1367] Q_out2[1368]
+ Q_out2[1369] Q_out2[1370] Q_out2[1371] Q_out2[1372] Q_out2[1373] Q_out2[1374] Q_out2[1375] Q_out2[1376]
+ Q_out2[1377] Q_out2[1378] Q_out2[1379] Q_out2[1380] Q_out2[1381] Q_out2[1382] Q_out2[1383] Q_out2[1384]
+ Q_out2[1385] Q_out2[1386] Q_out2[1387] Q_out2[1388] Q_out2[1389] Q_out2[1390] Q_out2[1391] Q_out2[1392]
+ Q_out2[1393] Q_out2[1394] Q_out2[1395] Q_out2[1396] Q_out2[1397] Q_out2[1398] Q_out2[1399] Q_out2[1400]
+ Q_out2[1401] Q_out2[1402] Q_out2[1403] Q_out2[1404] Q_out2[1405] Q_out2[1406] Q_out2[1407] Q_out2[1408]
+ Q_out2[1409] Q_out2[1410] Q_out2[1411] Q_out2[1412] Q_out2[1413] Q_out2[1414] Q_out2[1415] Q_out2[1416]
+ Q_out2[1417] Q_out2[1418] Q_out2[1419] Q_out2[1420] Q_out2[1421] Q_out2[1422] Q_out2[1423] Q_out2[1424]
+ Q_out2[1425] Q_out2[1426] Q_out2[1427] Q_out2[1428] Q_out2[1429] Q_out2[1430] Q_out2[1431] Q_out2[1432]
+ Q_out2[1433] Q_out2[1434] Q_out2[1435] Q_out2[1436] Q_out2[1437] Q_out2[1438] Q_out2[1439] Q_out2[1440]
+ Q_out2[1441] Q_out2[1442] Q_out2[1443] Q_out2[1444] Q_out2[1445] Q_out2[1446] Q_out2[1447] Q_out2[1448]
+ Q_out2[1449] Q_out2[1450] Q_out2[1451] Q_out2[1452] Q_out2[1453] Q_out2[1454] Q_out2[1455] Q_out2[1456]
+ Q_out2[1457] Q_out2[1458] Q_out2[1459] Q_out2[1460] Q_out2[1461] Q_out2[1462] Q_out2[1463] Q_out2[1464]
+ Q_out2[1465] Q_out2[1466] Q_out2[1467] Q_out2[1468] Q_out2[1469] Q_out2[1470] Q_out2[1471] Q_out2[1472]
+ Q_out2[1473] Q_out2[1474] Q_out2[1475] Q_out2[1476] Q_out2[1477] Q_out2[1478] Q_out2[1479] Q_out2[1480]
+ Q_out2[1481] Q_out2[1482] Q_out2[1483] Q_out2[1484] Q_out2[1485] Q_out2[1486] Q_out2[1487] Q_out2[1488]
+ Q_out2[1489] Q_out2[1490] Q_out2[1491] Q_out2[1492] Q_out2[1493] Q_out2[1494] Q_out2[1495] Q_out2[1496]
+ Q_out2[1497] Q_out2[1498] Q_out2[1499] Q_out2[1500] Q_out2[1501] Q_out2[1502] Q_out2[1503] Q_out2[1504]
+ Q_out2[1505] Q_out2[1506] Q_out2[1507] Q_out2[1508] Q_out2[1509] Q_out2[1510] Q_out2[1511] Q_out2[1512]
+ Q_out2[1513] Q_out2[1514] Q_out2[1515] Q_out2[1516] Q_out2[1517] Q_out2[1518] Q_out2[1519] Q_out2[1520]
+ Q_out2[1521] Q_out2[1522] Q_out2[1523] Q_out2[1524] Q_out2[1525] Q_out2[1526] Q_out2[1527] Q_out2[1528]
+ Q_out2[1529] Q_out2[1530] Q_out2[1531] Q_out2[1532] Q_out2[1533] Q_out2[1534] Q_out2[1535] Q_out2[1536]
+ Q_out2[1537] Q_out2[1538] Q_out2[1539] Q_out2[1540] Q_out2[1541] Q_out2[1542] Q_out2[1543] Q_out2[1544]
+ Q_out2[1545] Q_out2[1546] Q_out2[1547] Q_out2[1548] Q_out2[1549] Q_out2[1550] Q_out2[1551] Q_out2[1552]
+ Q_out2[1553] Q_out2[1554] Q_out2[1555] Q_out2[1556] Q_out2[1557] Q_out2[1558] Q_out2[1559] Q_out2[1560]
+ Q_out2[1561] Q_out2[1562] Q_out2[1563] Q_out2[1564] Q_out2[1565] Q_out2[1566] Q_out2[1567] Q_out2[1568]
+ Q_out2[1569] Q_out2[1570] Q_out2[1571] Q_out2[1572] Q_out2[1573] Q_out2[1574] Q_out2[1575] Q_out2[1576]
+ Q_out2[1577] Q_out2[1578] Q_out2[1579] Q_out2[1580] Q_out2[1581] Q_out2[1582] Q_out2[1583] Q_out2[1584]
+ Q_out2[1585] Q_out2[1586] Q_out2[1587] Q_out2[1588] Q_out2[1589] Q_out2[1590] Q_out2[1591] Q_out2[1592]
+ Q_out2[1593] Q_out2[1594] Q_out2[1595] Q_out2[1596] Q_out2[1597] Q_out2[1598] Q_out2[1599] Q_out2[1600]
+ Q_out2[1601] Q_out2[1602] Q_out2[1603] Q_out2[1604] Q_out2[1605] Q_out2[1606] Q_out2[1607] Q_out2[1608]
+ Q_out2[1609] Q_out2[1610] Q_out2[1611] Q_out2[1612] Q_out2[1613] Q_out2[1614] Q_out2[1615] Q_out2[1616]
+ Q_out2[1617] Q_out2[1618] Q_out2[1619] Q_out2[1620] Q_out2[1621] Q_out2[1622] Q_out2[1623] Q_out2[1624]
+ Q_out2[1625] Q_out2[1626] Q_out2[1627] Q_out2[1628] Q_out2[1629] Q_out2[1630] Q_out2[1631] Q_out2[1632]
+ D_out_row2[1] D_out_row2[2] D_out_row2[3] D_out_row2[4] D_out_row2[5] D_out_row2[6] D_out_row2[7] D_out_row2[8]
+ D_out_row2[9] D_out_row2[10] D_out_row2[11] D_out_row2[12] D_out_row2[13] D_out_row2[14] D_out_row2[15]
+ D_out_row2[16] D_out_row2[17] D_out_row2[18] D_out_row2[19] D_out_row2[20] D_out_row2[21] D_out_row2[22]
+ D_out_row2[23] D_out_row2[24] D_out_row2[25] D_out_row2[26] D_out_row2[27] D_out_row2[28] D_out_row2[29]
+ D_out_row2[30] D_out_row2[31] D_out_row2[32] D_out_row2[33] D_out_row2[34] D_out_row2[35] D_out_row2[36]
+ D_out_row2[37] D_out_row2[38] D_out_row2[39] D_out_row2[40] D_out_row2[41] D_out_row2[42] D_out_row2[43]
+ D_out_row2[44] D_out_row2[45] D_out_row2[46] D_out_row2[47] D_out_row2[48] D_out_row2[49] D_out_row2[50]
+ D_out_row2[51] D_out_row2[52] D_out_row2[53] D_out_row2[54] D_out_row2[55] D_out_row2[56] D_out_row2[57]
+ D_out_row2[58] D_out_row2[59] D_out_row2[60] D_out_row2[61] D_out_row2[62] D_out_row2[63] D_out_row2[64]
+ D_out_row2[65] D_out_row2[66] D_out_row2[67] swmatrix_68_by_25
x3 enable_in net3 VDDd VSSd PHI_CLK_buf
* noconn Q_out2[1:1632]
* noconn D_out_row2[1:67],D_out
* noconn Q_out[1:1488]
* noconn D_out_row[1:61],D_out1
**.ends
.end
